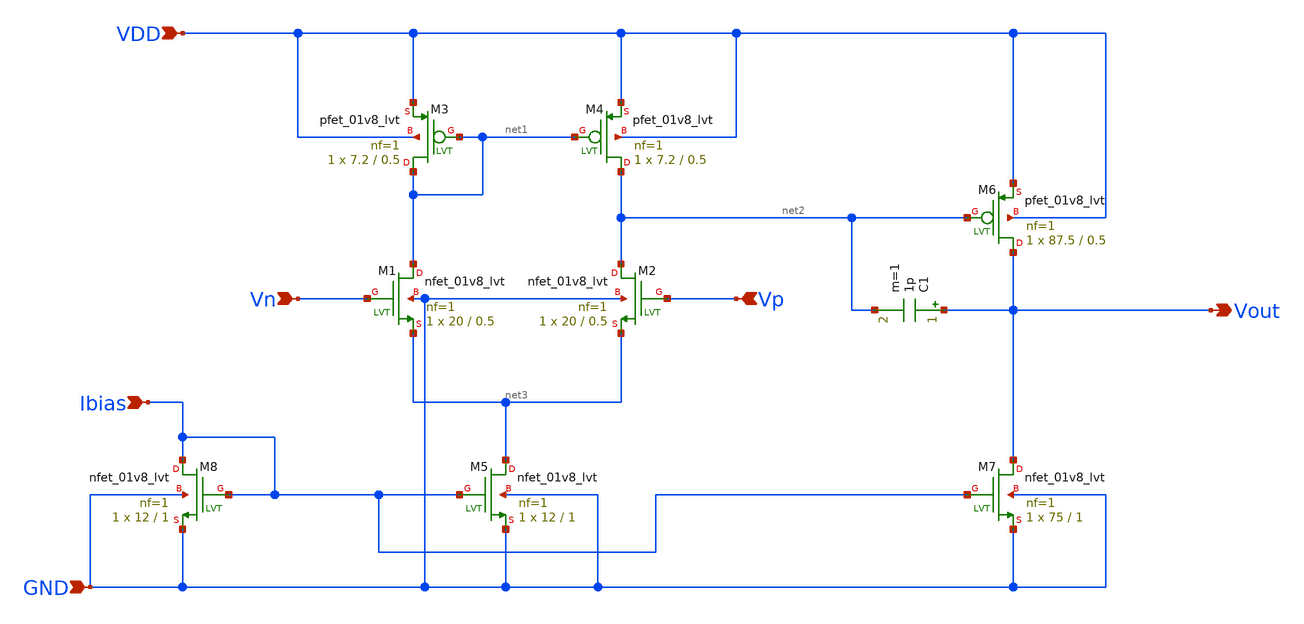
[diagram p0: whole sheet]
** sch_path: LDO/Schematic/Miller_OTA_NMOS_1.8v.sch
**.subckt Miller_OTA_NMOS_1.8v Ibias Vn Vp VDD GND Vout
*.ipin Ibias
*.ipin Vn
*.ipin Vp
*.ipin VDD
*.ipin GND
*.opin Vout
C1 Vout net2 1p m=1
XM1 net1 Vn net3 GND sky130_fd_pr__nfet_01v8_lvt L=0.5 W=20 nf=1 ad='int((nf+1)/2) * W/nf * 0.29' as='int((nf+2)/2) * W/nf * 0.29'
+ pd='2*int((nf+1)/2) * (W/nf + 0.29)' ps='2*int((nf+2)/2) * (W/nf + 0.29)' nrd='0.29 / W' nrs='0.29 / W'
+ sa=0 sb=0 sd=0 mult=1 m=1
XM2 net2 Vp net3 GND sky130_fd_pr__nfet_01v8_lvt L=0.5 W=20 nf=1 ad='int((nf+1)/2) * W/nf * 0.29' as='int((nf+2)/2) * W/nf * 0.29'
+ pd='2*int((nf+1)/2) * (W/nf + 0.29)' ps='2*int((nf+2)/2) * (W/nf + 0.29)' nrd='0.29 / W' nrs='0.29 / W'
+ sa=0 sb=0 sd=0 mult=1 m=1
XM5 net3 Ibias GND GND sky130_fd_pr__nfet_01v8_lvt L=1 W=12 nf=1 ad='int((nf+1)/2) * W/nf * 0.29' as='int((nf+2)/2) * W/nf * 0.29'
+ pd='2*int((nf+1)/2) * (W/nf + 0.29)' ps='2*int((nf+2)/2) * (W/nf + 0.29)' nrd='0.29 / W' nrs='0.29 / W'
+ sa=0 sb=0 sd=0 mult=1 m=1
XM8 Ibias Ibias GND GND sky130_fd_pr__nfet_01v8_lvt L=1 W=12 nf=1 ad='int((nf+1)/2) * W/nf * 0.29' as='int((nf+2)/2) * W/nf * 0.29'
+ pd='2*int((nf+1)/2) * (W/nf + 0.29)' ps='2*int((nf+2)/2) * (W/nf + 0.29)' nrd='0.29 / W' nrs='0.29 / W'
+ sa=0 sb=0 sd=0 mult=1 m=1
XM7 Vout Ibias GND GND sky130_fd_pr__nfet_01v8_lvt L=1 W=75 nf=1 ad='int((nf+1)/2) * W/nf * 0.29' as='int((nf+2)/2) * W/nf * 0.29'
+ pd='2*int((nf+1)/2) * (W/nf + 0.29)' ps='2*int((nf+2)/2) * (W/nf + 0.29)' nrd='0.29 / W' nrs='0.29 / W'
+ sa=0 sb=0 sd=0 mult=1 m=1
XM4 net2 net1 VDD VDD sky130_fd_pr__pfet_01v8_lvt L=0.5 W=7.2 nf=1 ad='int((nf+1)/2) * W/nf * 0.29' as='int((nf+2)/2) * W/nf * 0.29'
+ pd='2*int((nf+1)/2) * (W/nf + 0.29)' ps='2*int((nf+2)/2) * (W/nf + 0.29)' nrd='0.29 / W' nrs='0.29 / W'
+ sa=0 sb=0 sd=0 mult=1 m=1
XM3 net1 net1 VDD VDD sky130_fd_pr__pfet_01v8_lvt L=0.5 W=7.2 nf=1 ad='int((nf+1)/2) * W/nf * 0.29' as='int((nf+2)/2) * W/nf * 0.29'
+ pd='2*int((nf+1)/2) * (W/nf + 0.29)' ps='2*int((nf+2)/2) * (W/nf + 0.29)' nrd='0.29 / W' nrs='0.29 / W'
+ sa=0 sb=0 sd=0 mult=1 m=1
XM6 Vout net2 VDD VDD sky130_fd_pr__pfet_01v8_lvt L=0.5 W=87.5 nf=1 ad='int((nf+1)/2) * W/nf * 0.29'
+ as='int((nf+2)/2) * W/nf * 0.29' pd='2*int((nf+1)/2) * (W/nf + 0.29)' ps='2*int((nf+2)/2) * (W/nf + 0.29)'
+ nrd='0.29 / W' nrs='0.29 / W' sa=0 sb=0 sd=0 mult=1 m=1
**.ends
.end
